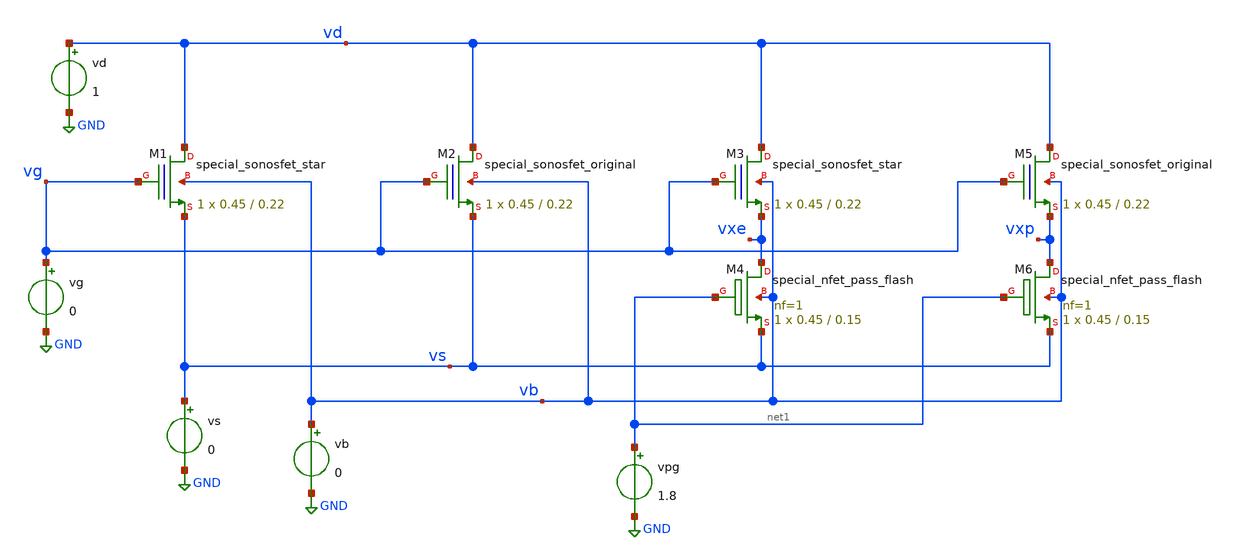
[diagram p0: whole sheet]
** sch_path: sonos/sonos_curves.sch
**.subckt sonos_curves
XM1 vd vg vs vb sky130_fd_bs_flash__special_sonosfet_star L=0.22 W=0.45 nf=1 ad='1 * W * 0.29' as='1 * W * 0.29'
+ pd='2 * (W + 0.29)' ps='2 * (W + 0.29)' nrd='0.29 / W' nrs='0.29 / W' sa=0 sb=0 sd=0 mult=1 m=1
XM2 vd vg vs vb sky130_fd_bs_flash__special_sonosfet_original L=0.22 W=0.45 nf=1 ad='1 * W * 0.29' as='1 * W * 0.29'
+ pd='2 * (W + 0.29)' ps='2 * (W + 0.29)' nrd='0.29 / W' nrs='0.29 / W' sa=0 sb=0 sd=0 mult=1 m=1
vg vg GND 0
vd vd GND 1
vs vs GND 0
vb vb GND 0
XM3 vd vg vxe vb sky130_fd_bs_flash__special_sonosfet_star L=0.22 W=0.45 nf=1 ad='1 * W * 0.29' as='1 * W * 0.29'
+ pd='2 * (W + 0.29)' ps='2 * (W + 0.29)' nrd='0.29 / W' nrs='0.29 / W' sa=0 sb=0 sd=0 mult=1 m=1
XM4 vxe net1 vs vb sky130_fd_pr__special_nfet_pass_flash L=0.15 W=0.45 nf=1 ad='1 * W * 0.29' as='1 * W * 0.29'
+ pd='2 * (W + 0.29)' ps='2 * (W + 0.29)' nrd='0.29 / W' nrs='0.29 / W' sa=0 sb=0 sd=0 mult=1 m=1
vpg net1 GND 1.8
XM6 vxp net1 vs vb sky130_fd_pr__special_nfet_pass_flash L=0.15 W=0.45 nf=1 ad='1 * W * 0.29' as='1 * W * 0.29'
+ pd='2 * (W + 0.29)' ps='2 * (W + 0.29)' nrd='0.29 / W' nrs='0.29 / W' sa=0 sb=0 sd=0 mult=1 m=1
XM5 vd vg vxp vb sky130_fd_bs_flash__special_sonosfet_original L=0.22 W=0.45 nf=1 ad='1 * W * 0.29' as='1 * W * 0.29'
+ pd='2 * (W + 0.29)' ps='2 * (W + 0.29)' nrd='0.29 / W' nrs='0.29 / W' sa=0 sb=0 sd=0 mult=1 m=1
**** begin user architecture code

** opencircuitdesign pdks install
.lib $::SKYWATER_MODELS/sky130.lib.spice tt
.include $::SKYWATER_MODELS/sonos_e/begin_of_life.spice
.include $::SKYWATER_MODELS/sonos_e/begin_of_life.pm3.spice
.include $::SKYWATER_MODELS/sonos_p/begin_of_life.spice
.include $::SKYWATER_MODELS/sonos_p/begin_of_life.pm3.spice



.option savecurrents
*.option abstol=1e-10 reltol=1e-2 chgtol=1e-12
*.ic v(bootp)=0 v(bootn)=0 v(inp)=0 v(inn)=0 v(inf)=0 v(inb)=0
*.ic v(net3)=0 v(net4)=0
.control
  unset appendwrite
  save all
  op
  remzerovec
  write test_sonos_curves.raw

  *tran 0.5n 2u
  dc vg -1.5 3 0.1 vd 0.1 2.1 0.5
  remzerovec
  write test_sonos_curves.raw

  dc vd 0 2 0.1 vg -1.5 3 0.5
  remzerovec
  write test_sonos_curves_gvd.raw
.endc


**** end user architecture code
**.ends
.GLOBAL GND
.end
